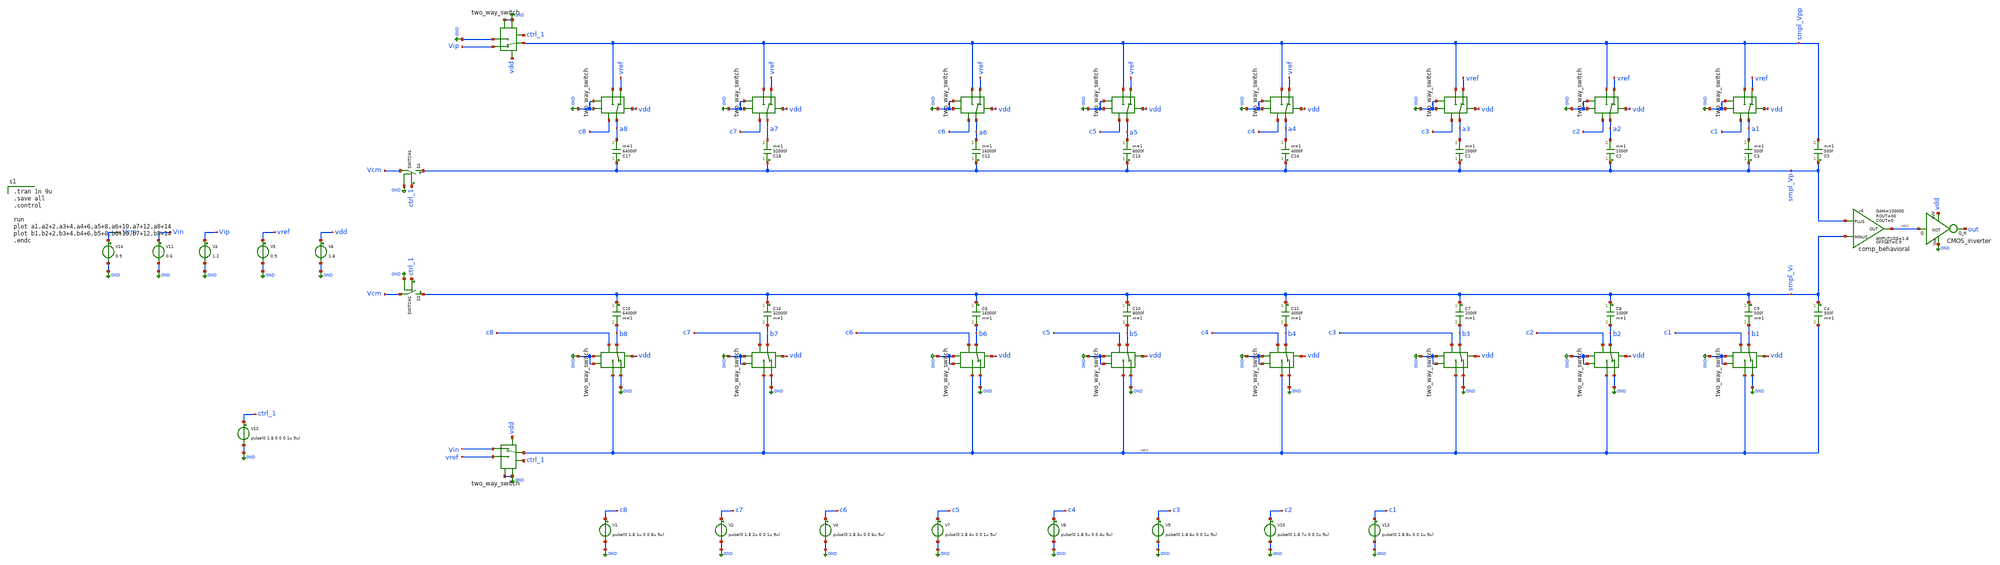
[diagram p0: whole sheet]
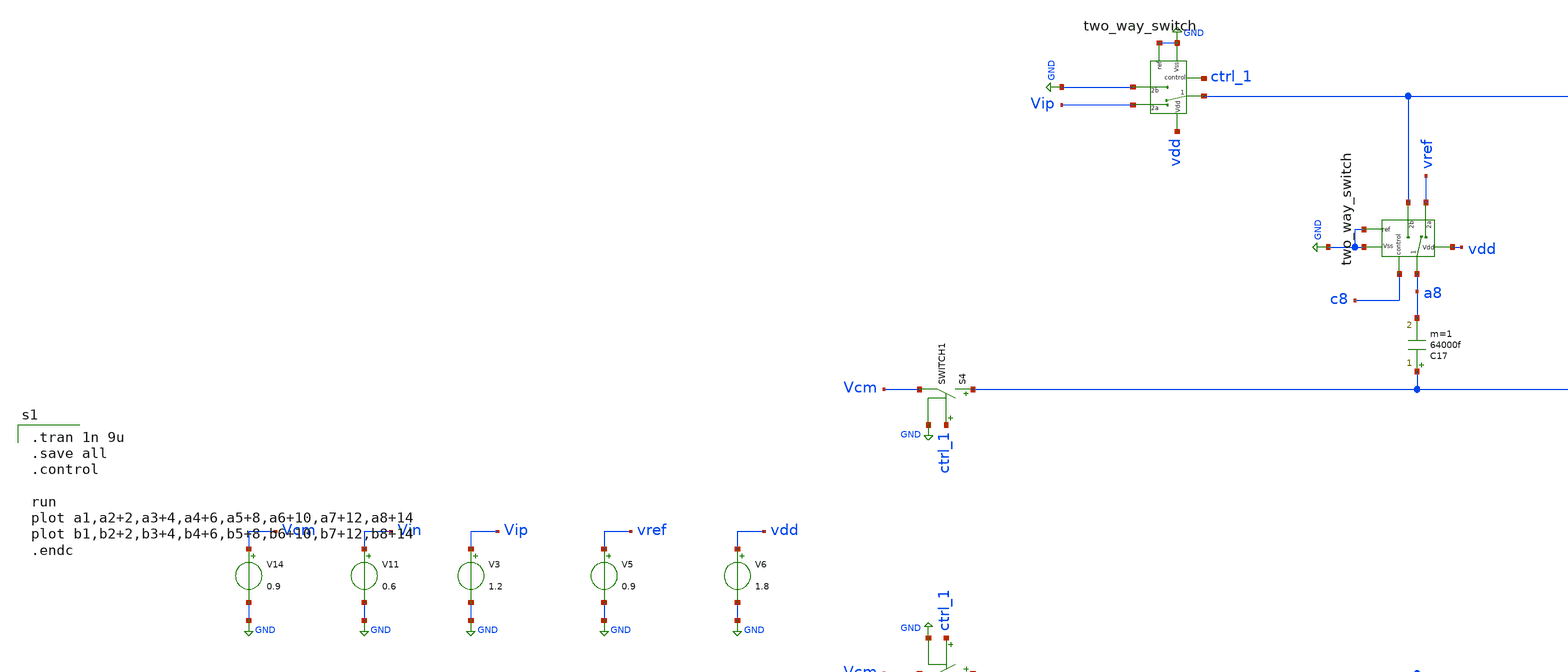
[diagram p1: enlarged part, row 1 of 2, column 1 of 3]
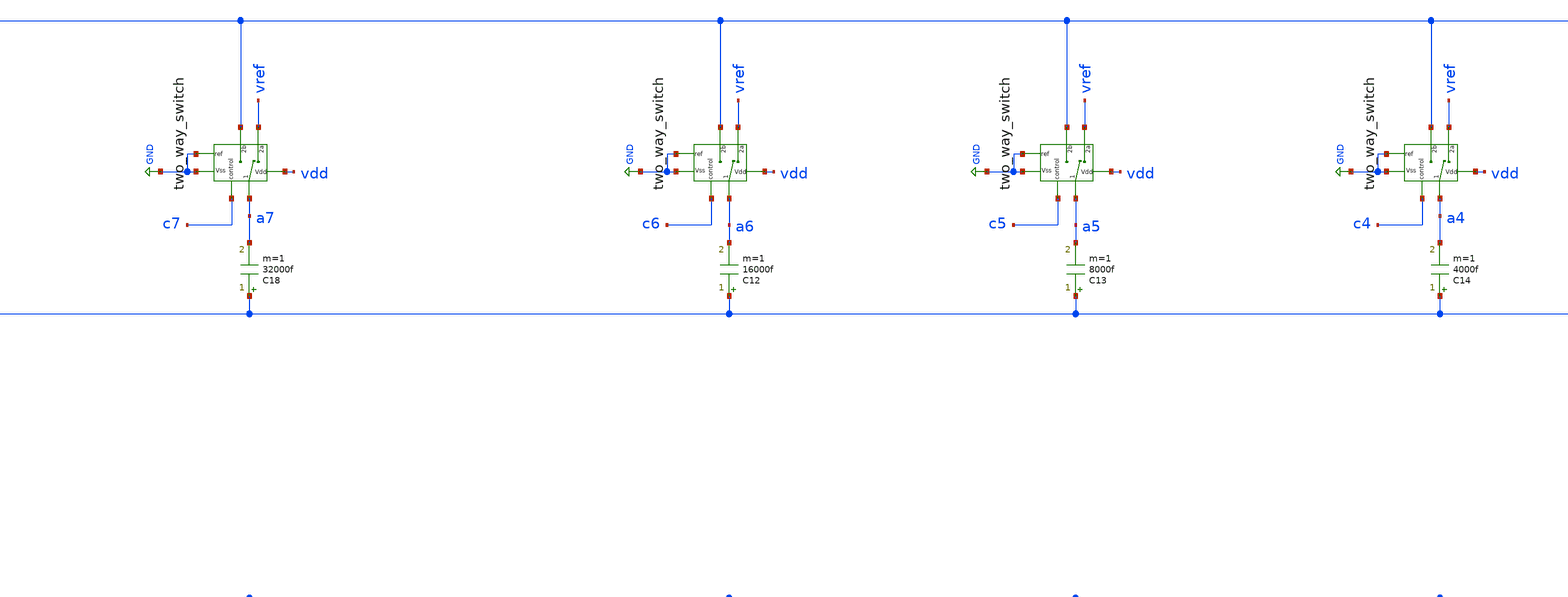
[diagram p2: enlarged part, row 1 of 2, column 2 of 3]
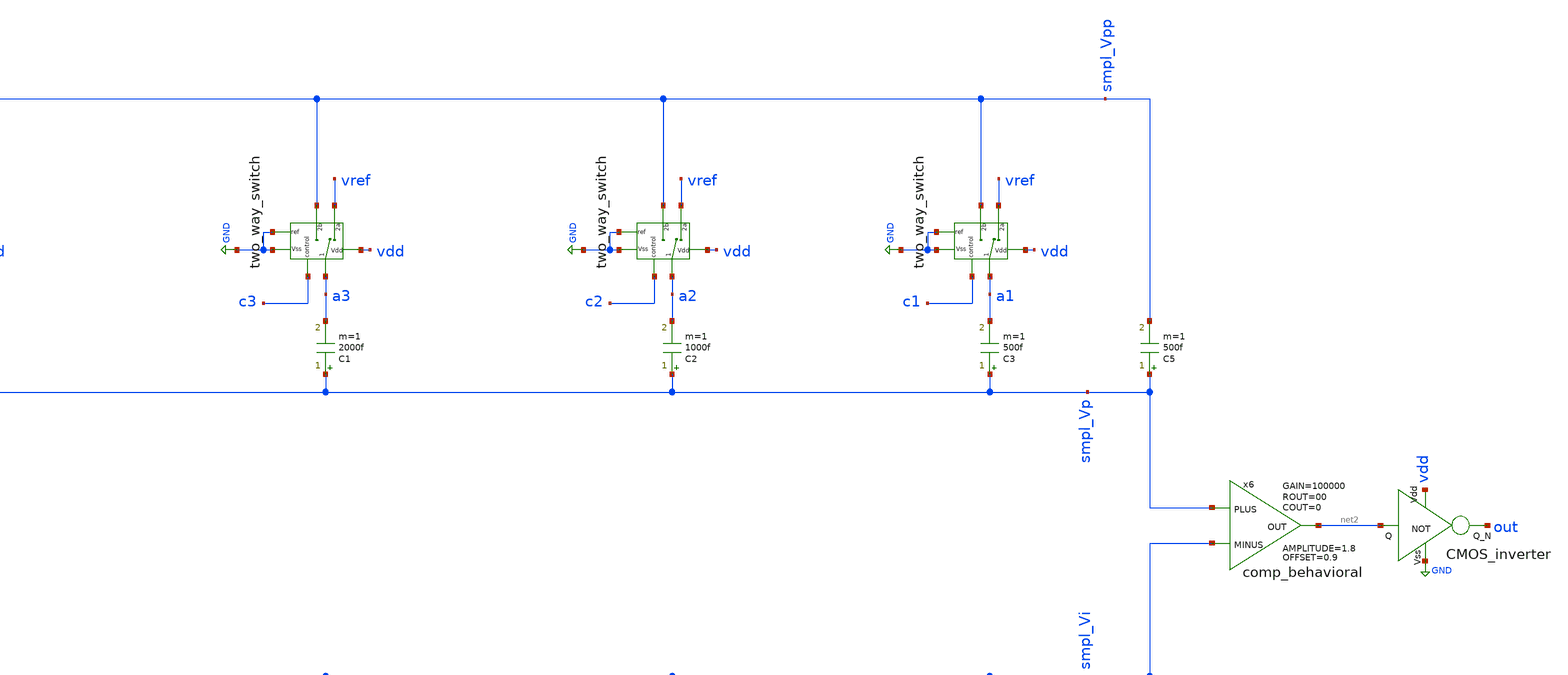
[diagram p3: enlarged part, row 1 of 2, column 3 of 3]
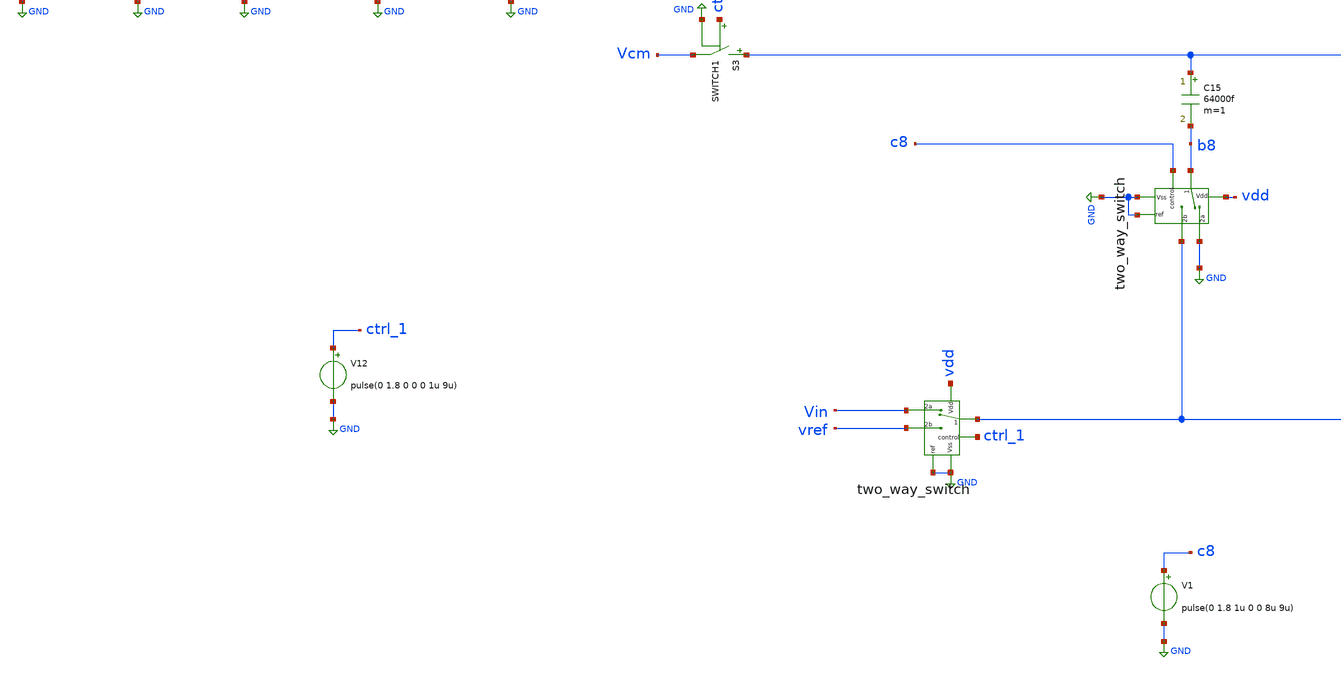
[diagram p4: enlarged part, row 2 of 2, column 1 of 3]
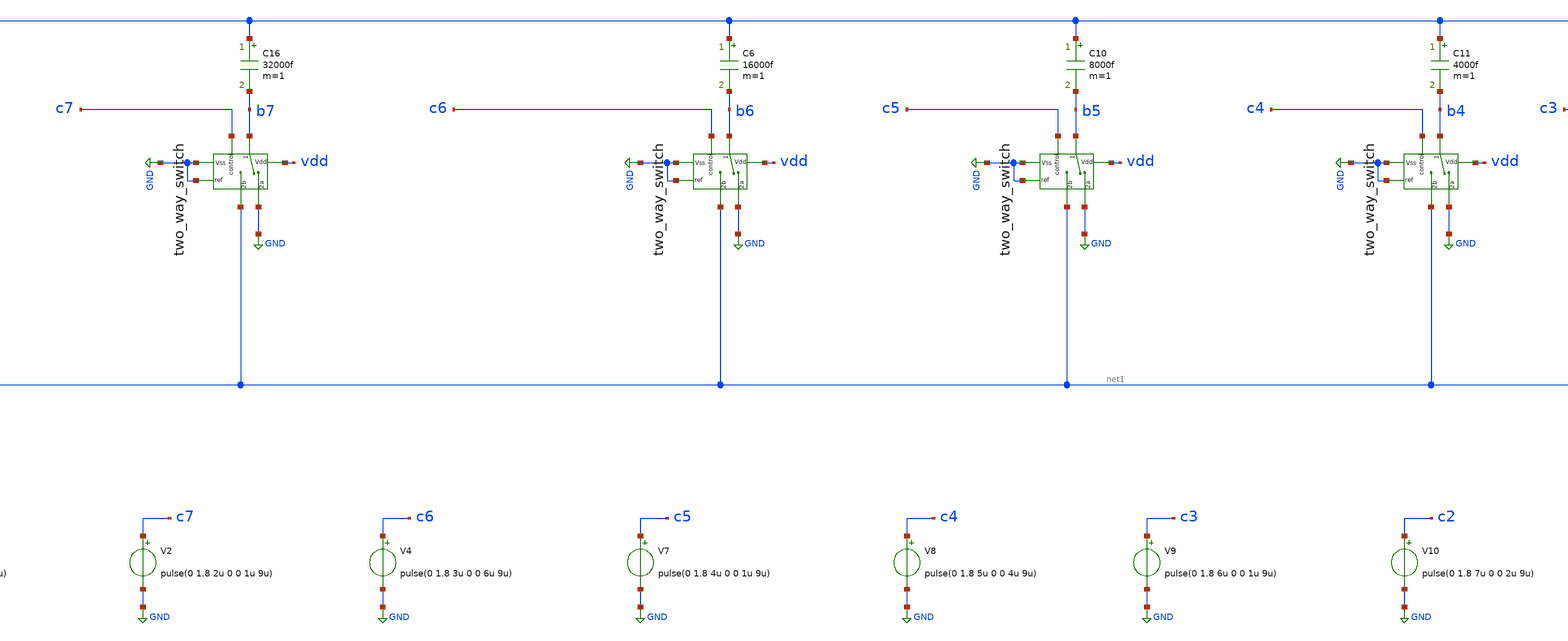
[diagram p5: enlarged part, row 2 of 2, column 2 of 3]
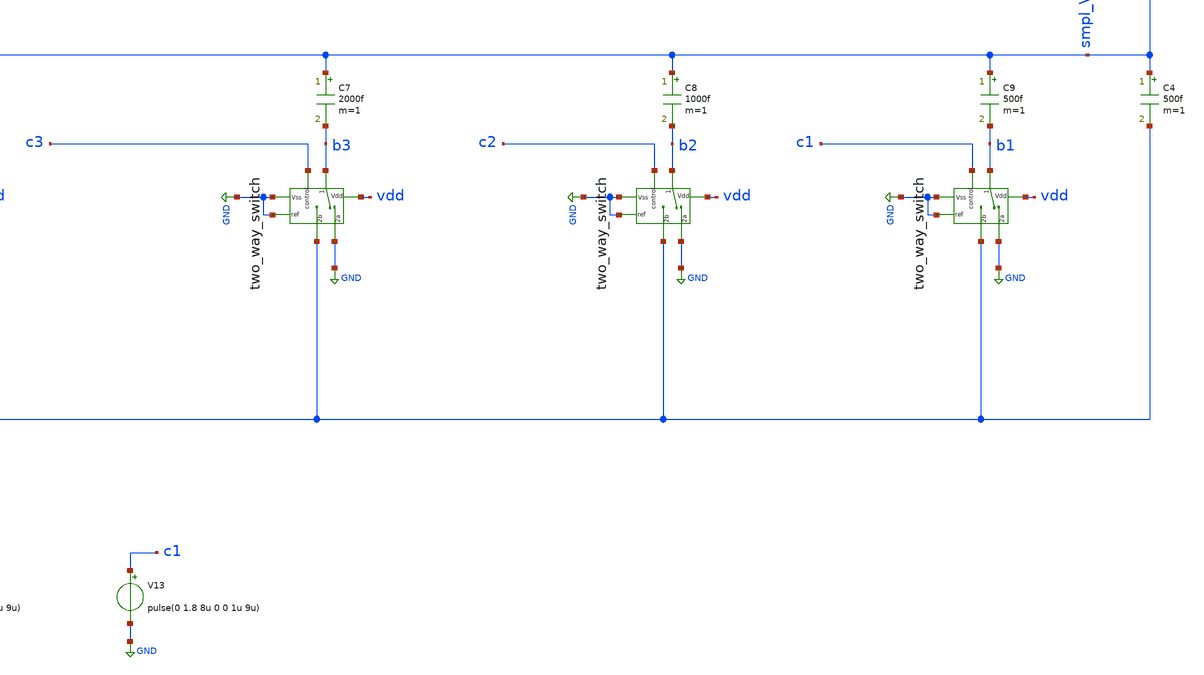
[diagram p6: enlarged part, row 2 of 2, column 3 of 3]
** sch_path: Behavioral_model/test.sch
.lib $::SKYWATER_MODELS/sky130.lib.spice tt
.include $::SKYWATER_STDCELLS/sky130_fd_sc_hd.spice
.model switch1 sw vt=0.5 vh=0 ron=0.1 roff=10000G

**.subckt test
S3 smpl_Vi Vcm ctrl_1 GND SWITCH1
V3 Vip GND 1.2
C7 smpl_Vi b3 2000f m=1
x7 b3 vdd c3 GND GND net1 GND two_way_switch
C8 smpl_Vi b2 1000f m=1
C9 smpl_Vi b1 500f m=1
x1 b2 vdd c2 GND GND net1 GND two_way_switch
x2 b1 vdd c1 GND GND net1 GND two_way_switch
V5 vref GND 0.9
V6 vdd GND 1.8
S4 smpl_Vp Vcm ctrl_1 GND SWITCH1
C1 smpl_Vp a3 2000f m=1
x3 a3 vdd c3 GND vref smpl_Vpp GND two_way_switch
C2 smpl_Vp a2 1000f m=1
C3 smpl_Vp a1 500f m=1
x4 a2 vdd c2 GND vref smpl_Vpp GND two_way_switch
x5 a1 vdd c1 GND vref smpl_Vpp GND two_way_switch
x6 smpl_Vp smpl_Vi net2 comp_behavioral OFFSET=0.9 AMPLITUDE=1.8 GAIN=100000 ROUT=00 COUT=0
V11 Vin GND 0.6
C4 smpl_Vi net1 500f m=1
C5 smpl_Vp smpl_Vpp 500f m=1
C6 smpl_Vi b6 16000f m=1
x11 b6 vdd c6 GND GND net1 GND two_way_switch
C10 smpl_Vi b5 8000f m=1
C11 smpl_Vi b4 4000f m=1
x12 b5 vdd c5 GND GND net1 GND two_way_switch
x13 b4 vdd c4 GND GND net1 GND two_way_switch
C12 smpl_Vp a6 16000f m=1
x14 a6 vdd c6 GND vref smpl_Vpp GND two_way_switch
C13 smpl_Vp a5 8000f m=1
C14 smpl_Vp a4 4000f m=1
x15 a5 vdd c5 GND vref smpl_Vpp GND two_way_switch
x16 a4 vdd c4 GND vref smpl_Vpp GND two_way_switch
C15 smpl_Vi b8 64000f m=1
x20 b8 vdd c8 GND GND net1 GND two_way_switch
C16 smpl_Vi b7 32000f m=1
x21 b7 vdd c7 GND GND net1 GND two_way_switch
C17 smpl_Vp a8 64000f m=1
x22 a8 vdd c8 GND vref smpl_Vpp GND two_way_switch
C18 smpl_Vp a7 32000f m=1
x23 a7 vdd c7 GND vref smpl_Vpp GND two_way_switch
x26 smpl_Vpp vdd ctrl_1 GND Vip GND GND two_way_switch
x27 net1 vdd ctrl_1 GND Vin vref GND two_way_switch
V14 Vcm GND 0.9
V12 ctrl_1 GND pulse(0 1.8 0 0 0 1u 9u)
x10 vdd net2 out GND CMOS_inverter
V1 c8 GND pulse(0 1.8 1u 0 0 8u 9u)
V2 c7 GND pulse(0 1.8 2u 0 0 1u 9u)
V4 c6 GND pulse(0 1.8 3u 0 0 6u 9u)
V7 c5 GND pulse(0 1.8 4u 0 0 1u 9u)
V8 c4 GND pulse(0 1.8 5u 0 0 4u 9u)
V9 c3 GND pulse(0 1.8 6u 0 0 1u 9u)
V10 c2 GND pulse(0 1.8 7u 0 0 2u 9u)
V13 c1 GND pulse(0 1.8 8u 0 0 1u 9u)
**** begin user architecture code

.tran 1n 9u
.save all
.control

run
plot a1,a2+2,a3+4,a4+6,a5+8,a6+10,a7+12,a8+14
plot b1,b2+2,b3+4,b4+6,b5+8,b6+10,b7+12,b8+14
.endc

**** end user architecture code
**.ends

* expanding   symbol:  two_way_switch.sym # of pins=7
** sym_path: Behavioral_model/two_way_switch.sym
** sch_path: Behavioral_model/two_way_switch.sch
.subckt two_way_switch 1 Vdd control ref 2a 2b Vss
*.iopin 2b
*.iopin 2a
*.ipin ref
*.iopin 1
*.ipin Vdd
*.ipin Vss
*.ipin control
S1 1 2a control ref SWITCH1
S2 1 2b net1 ref SWITCH1
x1 Vdd control net1 Vss CMOS_inverter
.ends


* expanding   symbol:  comp_behavioral.sym # of pins=3
** sym_path: Behavioral_model/comp_behavioral.sym
** sch_path: Behavioral_model/comp_behavioral.sch
.subckt comp_behavioral PLUS MINUS OUT  OFFSET=0.9 AMPLITUDE=0.9 GAIN=100000 ROUT=00 COUT=0
*.ipin PLUS
*.ipin MINUS
*.opin OUT
B1 IOUT 0 V = {OFFSET + AMPLITUDE/2*(tanh(V(IPLUS,IMINUS)*GAIN*2/AMPLITUDE))}
V1 IPLUS PLUS 3
V2 IMINUS MINUS 3
R1 OUT IOUT {ROUT} m=1
C3 OUT 0 {COUT} m=1
.ends


* expanding   symbol:  CMOS_inverter.sym # of pins=4
** sym_path: Behavioral_model/CMOS_inverter.sym
** sch_path: Behavioral_model/CMOS_inverter.sch
.subckt CMOS_inverter Vdd Q Q_N Vss
*.ipin Q
*.ipin Vdd
*.ipin Vss
*.opin Q_N
XM1 Q_N Q Vss Vss sky130_fd_pr__nfet_01v8 L=0.15 W=1 nf=1 ad='int((nf+1)/2) * W/nf * 0.29' as='int((nf+2)/2) * W/nf * 0.29'
+ pd='2*int((nf+1)/2) * (W/nf + 0.29)' ps='2*int((nf+2)/2) * (W/nf + 0.29)' nrd='0.29 / W' nrs='0.29 / W'
+ sa=0 sb=0 sd=0 mult=1 m=1
XM3 Q_N Q Vdd Vdd sky130_fd_pr__pfet_01v8 L=0.15 W=1 nf=1 ad='int((nf+1)/2) * W/nf * 0.29' as='int((nf+2)/2) * W/nf * 0.29'
+ pd='2*int((nf+1)/2) * (W/nf + 0.29)' ps='2*int((nf+2)/2) * (W/nf + 0.29)' nrd='0.29 / W' nrs='0.29 / W'
+ sa=0 sb=0 sd=0 mult=1 m=1
.ends

.GLOBAL GND
.end
